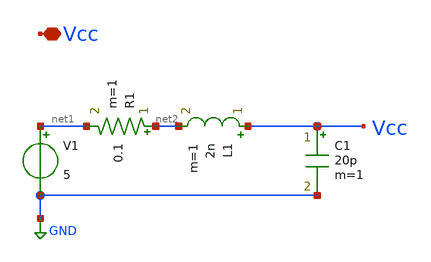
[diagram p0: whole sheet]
** sch_path: Git Files/Simulation Schematic/newVcc_5.sch
**.subckt newVcc_5 Vcc
*.iopin Vcc
V1 net1 GND 5
R1 net2 net1 0.1 m=1
L1 Vcc net2 2n m=1
C1 Vcc GND 20p m=1
**.ends
.GLOBAL GND
.end
